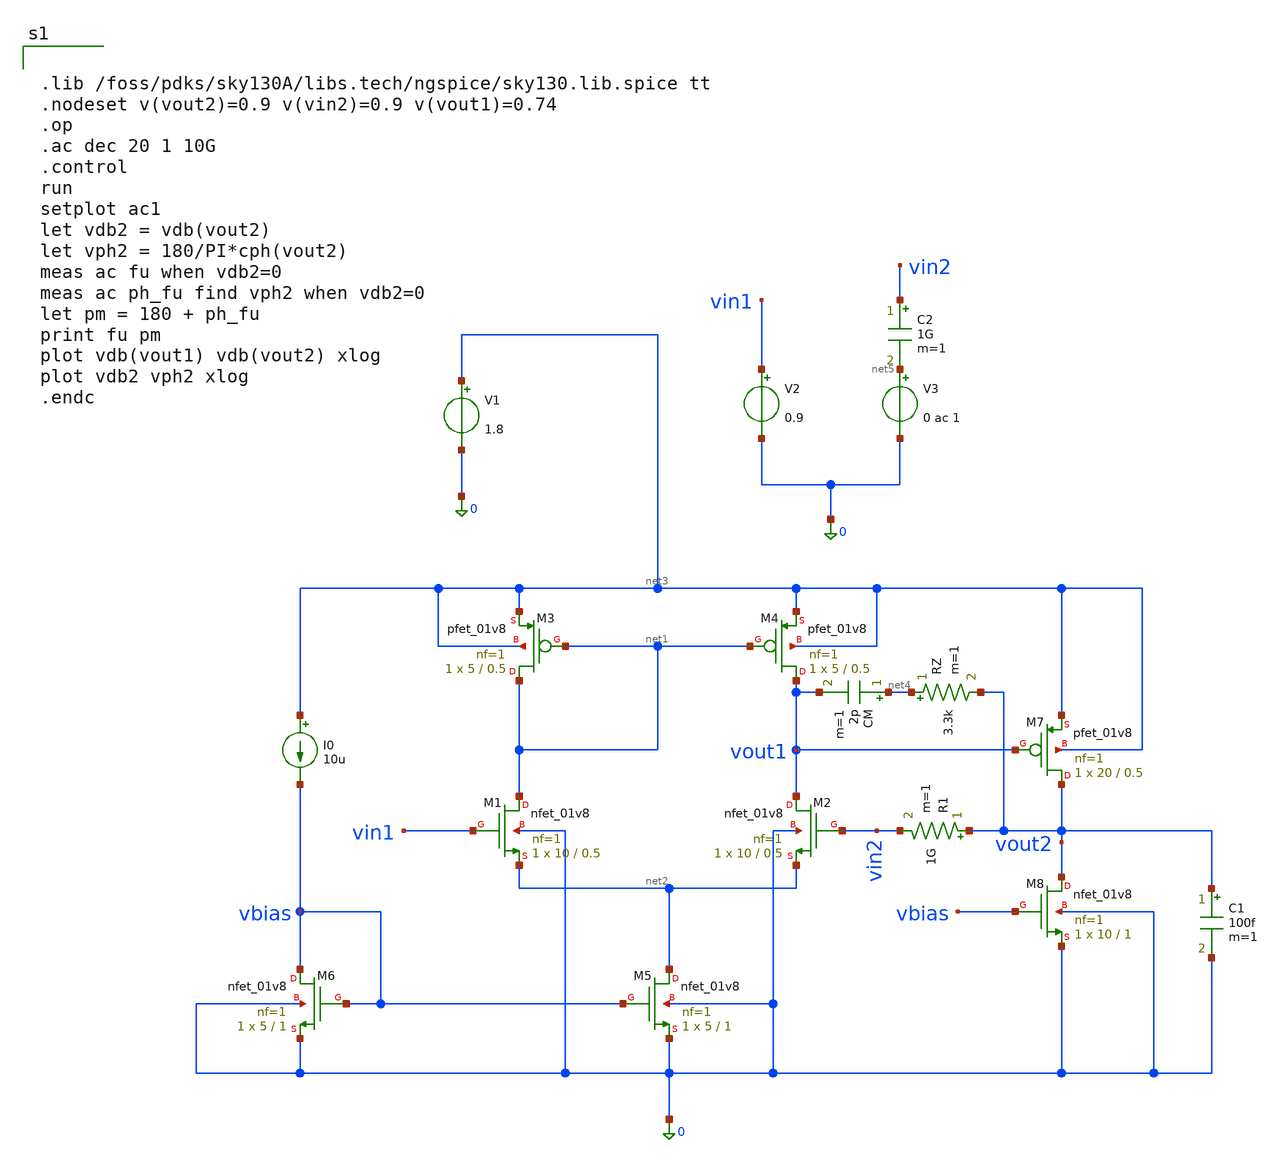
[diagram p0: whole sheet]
** sch_path: src/schematics/two_stage_ota.sch
**.subckt two_stage_ota
XM1 net1 vin1 net2 0 sky130_fd_pr__nfet_01v8 L=0.5 W=10 nf=1 ad='int((1 + 1)/2) * 10 / 1 * 0.29' as='int((1 + 2)/2) * 10 / 1 * 0.29'
+ pd='2*int((1 + 1)/2) * (10 / 1 + 0.29)' ps='2*int((1 + 2)/2) * (10 / 1 + 0.29)' nrd='0.29 / 10 ' nrs='0.29 / 10 '
+ sa=0 sb=0 sd=0 mult=1 m=1
XM2 vout1 vin2 net2 0 sky130_fd_pr__nfet_01v8 L=0.5 W=10 nf=1 ad='int((1 + 1)/2) * 10 / 1 * 0.29' as='int((1 + 2)/2) * 10 / 1 * 0.29'
+ pd='2*int((1 + 1)/2) * (10 / 1 + 0.29)' ps='2*int((1 + 2)/2) * (10 / 1 + 0.29)' nrd='0.29 / 10 ' nrs='0.29 / 10 '
+ sa=0 sb=0 sd=0 mult=1 m=1
XM3 net1 net1 net3 net3 sky130_fd_pr__pfet_01v8 L=0.5 W=5 nf=1 ad='int((1 + 1)/2) * 5 / 1 * 0.29' as='int((1 + 2)/2) * 5 / 1 * 0.29'
+ pd='2*int((1 + 1)/2) * (5 / 1 + 0.29)' ps='2*int((1 + 2)/2) * (5 / 1 + 0.29)' nrd='0.29 / 5 ' nrs='0.29 / 5 '
+ sa=0 sb=0 sd=0 mult=1 m=1
XM4 vout1 net1 net3 net3 sky130_fd_pr__pfet_01v8 L=0.5 W=5 nf=1 ad='int((1 + 1)/2) * 5 / 1 * 0.29' as='int((1 + 2)/2) * 5 / 1 * 0.29'
+ pd='2*int((1 + 1)/2) * (5 / 1 + 0.29)' ps='2*int((1 + 2)/2) * (5 / 1 + 0.29)' nrd='0.29 / 5 ' nrs='0.29 / 5 '
+ sa=0 sb=0 sd=0 mult=1 m=1
XM5 net2 vbias 0 0 sky130_fd_pr__nfet_01v8 L=1 W=5 nf=1 ad='int((1 + 1)/2) * 5 / 1 * 0.29' as='int((1 + 2)/2) * 5 / 1 * 0.29'
+ pd='2*int((1 + 1)/2) * (5 / 1 + 0.29)' ps='2*int((1 + 2)/2) * (5 / 1 + 0.29)' nrd='0.29 / 5 ' nrs='0.29 / 5 '
+ sa=0 sb=0 sd=0 mult=1 m=1
XM6 vbias vbias 0 0 sky130_fd_pr__nfet_01v8 L=1 W=5 nf=1 ad='int((1 + 1)/2) * 5 / 1 * 0.29' as='int((1 + 2)/2) * 5 / 1 * 0.29'
+ pd='2*int((1 + 1)/2) * (5 / 1 + 0.29)' ps='2*int((1 + 2)/2) * (5 / 1 + 0.29)' nrd='0.29 / 5 ' nrs='0.29 / 5 '
+ sa=0 sb=0 sd=0 mult=1 m=1
I0 net3 vbias 10u
C1 vout2 0 100f m=1
V1 net3 0 1.8
V2 vin1 0 0.9
V3 net5 0 0 ac 1
XM7 vout2 vout1 net3 net3 sky130_fd_pr__pfet_01v8 L=0.5 W=20 nf=1 ad='int((1 + 1)/2) * 20 / 1 * 0.29'
+ as='int((1 + 2)/2) * 20 / 1 * 0.29' pd='2*int((1 + 1)/2) * (20 / 1 + 0.29)' ps='2*int((1 + 2)/2) * (20 / 1 + 0.29)'
+ nrd='0.29 / 20 ' nrs='0.29 / 20 ' sa=0 sb=0 sd=0 mult=1 m=1
XM8 vout2 vbias 0 0 sky130_fd_pr__nfet_01v8 L=1 W=10 nf=1 ad='int((1 + 1)/2) * 10 / 1 * 0.29' as='int((1 + 2)/2) * 10 / 1 * 0.29'
+ pd='2*int((1 + 1)/2) * (10 / 1 + 0.29)' ps='2*int((1 + 2)/2) * (10 / 1 + 0.29)' nrd='0.29 / 10 ' nrs='0.29 / 10 '
+ sa=0 sb=0 sd=0 mult=1 m=1
R1 vout2 vin2 1G m=1
C2 vin2 net5 1G m=1
CM net4 vout1 2p m=1
RZ net4 vout2 3.3k m=1
**** begin user architecture code


.lib /foss/pdks/sky130A/libs.tech/ngspice/sky130.lib.spice tt
.nodeset v(vout2)=0.9 v(vin2)=0.9 v(vout1)=0.74
.op
.ac dec 20 1 10G
.control
run
setplot ac1
let vdb2 = vdb(vout2)
let vph2 = 180/PI*cph(vout2)
meas ac fu when vdb2=0
meas ac ph_fu find vph2 when vdb2=0
let pm = 180 + ph_fu
print fu pm
plot vdb(vout1) vdb(vout2) xlog
plot vdb2 vph2 xlog
.endc


**** end user architecture code
**.ends
.end
